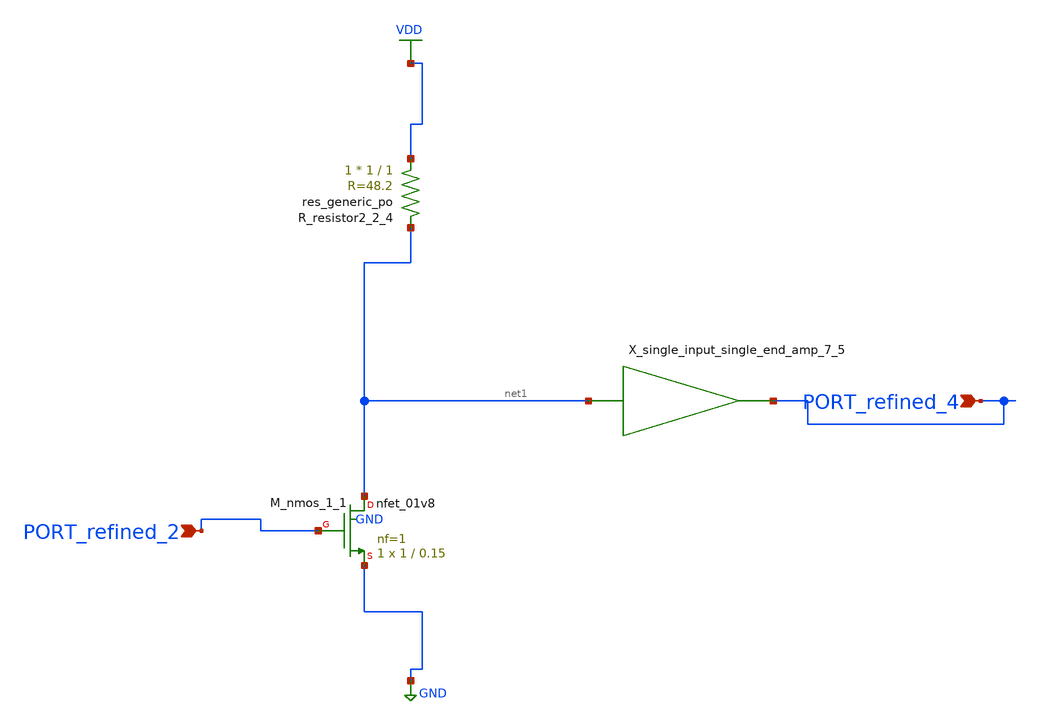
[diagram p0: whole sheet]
** sch_path: schematics/AMSNet/439.sch
**.subckt 439 PORT_refined_2 PORT_refined_4
*.ipin PORT_refined_2
*.ipin PORT_refined_4
XM_nmos_1_1 net1 PORT_refined_2 GND GND sky130_fd_pr__nfet_01v8 L=0.15 W=1 nf=1 ad='int((1 + 1)/2) * 1 / 1 * 0.29'
+ as='int((1 + 2)/2) * 1 / 1 * 0.29' pd='2*int((1 + 1)/2) * (1 / 1 + 0.29)' ps='2*int((1 + 2)/2) * (1 / 1 + 0.29)'
+ nrd='0.29 / 1 ' nrs='0.29 / 1 ' sa=0 sb=0 sd=0 mult=1 m=1
XR_resistor2_2_4 VDD net1 sky130_fd_pr__res_generic_po W=1 L=1 m=1
X_single_input_single_end_amp_7_5 net1 PORT_refined_4 schemgen_siso_amp
**.ends

* expanding   symbol:  schemgen_siso_amp.sym # of pins=2
** sym_path: symbols/schemgen_siso_amp.sym
.subckt schemgen_siso_amp IN OUT
* SchemGen ideal single-input amplifier: Vout = 1e5 * V(IN)
E1 OUT 0 IN 0 1e5
.ends schemgen_siso_amp
.GLOBAL GND
.GLOBAL VDD
.end
